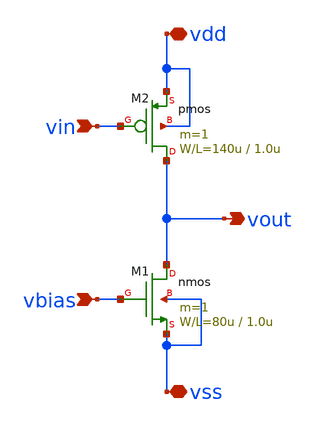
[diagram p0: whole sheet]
** sch_path: member_project/GroupWork/Team_masahiro/pfet_common_source_load_current.sch
**.subckt pfet_common_source_load_current vss vdd vin vout vbias
*.iopin vss
*.iopin vdd
*.ipin vin
*.opin vout
*.ipin vbias
M1 vout vbias vss vss nmos L=1.0u W=80u m=1
M2 vout vin vdd vdd pmos L=1.0u W=140u m=1
**** begin user architecture code
 .include $::LIB/mos.lib
.include $::LIB/passive.lib
.include $::LIB/diode.lib
**** end user architecture code
**.ends
.end
